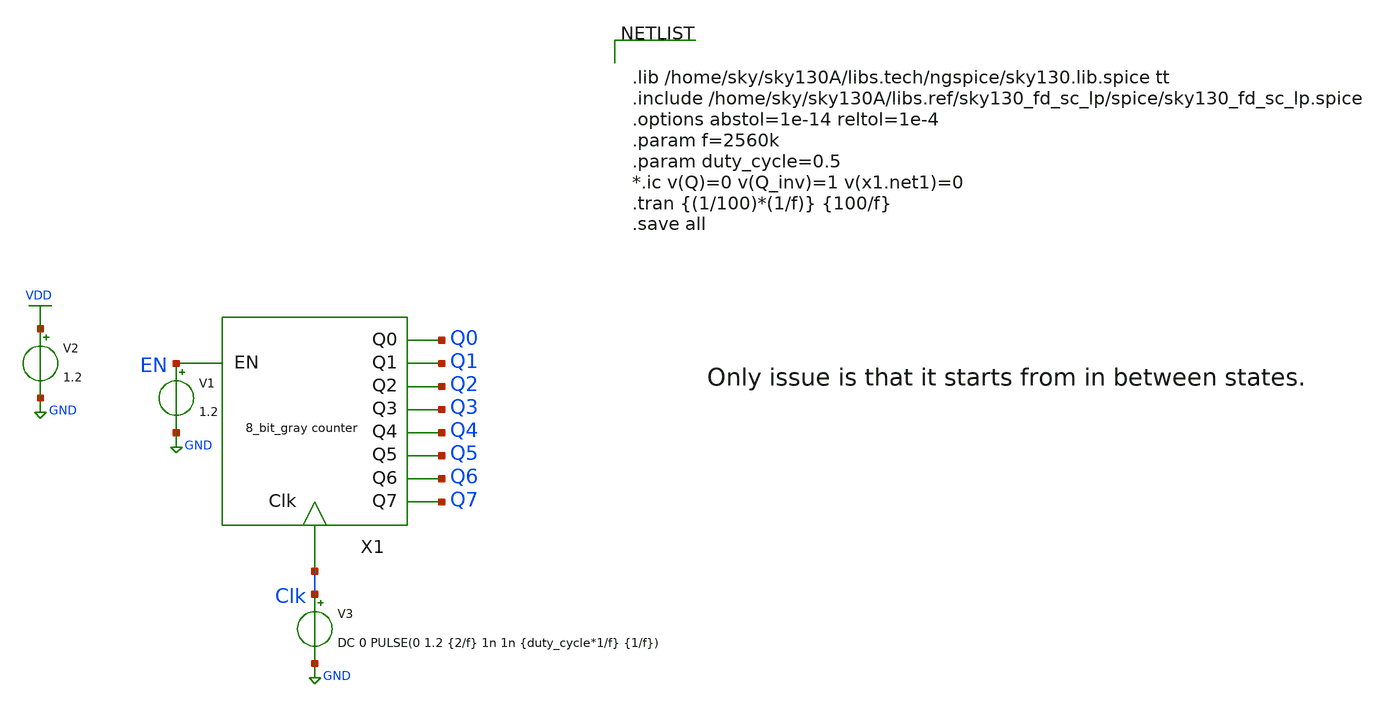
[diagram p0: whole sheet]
** sch_path: xschem/8_bit_gray_counter/8_bit_gray_counter_tb.sch
**.subckt 8_bit_gray_counter_tb
X1 EN Q1 Q6 Clk Q0 Q2 Q3 Q4 Q5 Q7 8_bit_gray_counter
V3 Clk GND DC 0 PULSE(0 1.2 {2/f} 1n 1n {duty_cycle*1/f} {1/f})
V1 EN GND 1.2
V2 VDD GND 1.2
**** begin user architecture code


.lib /home/sky/sky130A/libs.tech/ngspice/sky130.lib.spice tt
.include /home/sky/sky130A/libs.ref/sky130_fd_sc_lp/spice/sky130_fd_sc_lp.spice
.options abstol=1e-14 reltol=1e-4
.param f=2560k
.param duty_cycle=0.5
*.ic v(Q)=0 v(Q_inv)=1 v(x1.net1)=0
.tran {(1/100)*(1/f)} {100/f}
.save all


**** end user architecture code
**.ends

* expanding   symbol:  8_bit_gray_counter/8_bit_gray_counter.sym # of pins=10
** sym_path: xschem/8_bit_gray_counter/8_bit_gray_counter.sym
** sch_path: xschem/8_bit_gray_counter/8_bit_gray_counter.sch
.subckt 8_bit_gray_counter EN Q1 Q6 Clk Q0 Q2 Q3 Q4 Q5 Q7
*.ipin Clk
*.ipin EN
*.opin Q0
*.opin Q1
*.opin Q2
*.opin Q3
*.opin Q4
*.opin Q5
*.opin Q6
*.opin Q7
*.ipin Clk
*.ipin EN
*.opin Q0
*.opin Q1
*.opin Q2
*.opin Q3
*.opin Q4
*.opin Q5
*.opin Q6
*.opin Q7
X1 EN qb0 net7 Clk T_flip_flop
X2 qb0 qb1 net8 Clk T_flip_flop
X3 net1 qb2 net9 Clk T_flip_flop
X4 net2 qb3 net10 Clk T_flip_flop
X5 net3 qb4 net11 Clk T_flip_flop
X6 net4 qb5 net12 Clk T_flip_flop
X7 net5 qb6 net13 Clk T_flip_flop
X8 net6 Q7 net14 Clk T_flip_flop
X10 qb0 qb1 net1 and_gate
X11 net1 qb2 net2 and_gate
X12 net2 qb3 net3 and_gate
X13 net3 qb4 net4 and_gate
X14 net4 qb5 net5 and_gate
X15 net5 qb6 net6 and_gate
X16 qb0 qb1 Q0 exor_gate
X17 qb1 qb2 Q1 exor_gate
X18 qb2 qb3 Q2 exor_gate
X19 qb3 qb4 Q3 exor_gate
X20 qb4 qb5 Q4 exor_gate
X21 qb5 qb6 Q5 exor_gate
X22 qb6 Q7 Q6 exor_gate
X9 EN qb0 net7 Clk T_flip_flop
X23 qb0 qb1 net8 Clk T_flip_flop
X24 net1 qb2 net9 Clk T_flip_flop
X25 net2 qb3 net10 Clk T_flip_flop
X26 net3 qb4 net11 Clk T_flip_flop
X27 net4 qb5 net12 Clk T_flip_flop
X28 net5 qb6 net13 Clk T_flip_flop
X29 net6 Q7 net14 Clk T_flip_flop
X30 qb0 qb1 net1 and_gate
X31 net1 qb2 net2 and_gate
X32 net2 qb3 net3 and_gate
X33 net3 qb4 net4 and_gate
X34 net4 qb5 net5 and_gate
X35 net5 qb6 net6 and_gate
X36 qb0 qb1 Q0 exor_gate
X37 qb1 qb2 Q1 exor_gate
X38 qb2 qb3 Q2 exor_gate
X39 qb3 qb4 Q3 exor_gate
X40 qb4 qb5 Q4 exor_gate
X41 qb5 qb6 Q5 exor_gate
X42 qb6 Q7 Q6 exor_gate
.ends


* expanding   symbol:  T_flip_flop/T_flip_flop.sym # of pins=4
** sym_path: xschem/T_flip_flop/T_flip_flop.sym
** sch_path: xschem/T_flip_flop/T_flip_flop.sch
.subckt T_flip_flop T Q Q_inv Clk
*.ipin T
*.ipin Clk
*.opin Q
*.opin Q_inv
X1 net1 Q Q_inv Clk d_flip_flop
X2 Q T net1 exor_gate
.ends


* expanding   symbol:  and_gate/and_gate.sym # of pins=3
** sym_path: xschem/and_gate/and_gate.sym
** sch_path: xschem/and_gate/and_gate.sch
.subckt and_gate A B out
*.ipin A
*.ipin B
*.opin out
XM1 net1 A net2 GND sky130_fd_pr__nfet_01v8 L=0.18 W=1 nf=1 ad='int((nf+1)/2) * W/nf * 0.29' as='int((nf+2)/2) * W/nf * 0.29'
+ pd='2*int((nf+1)/2) * (W/nf + 0.29)' ps='2*int((nf+2)/2) * (W/nf + 0.29)' nrd='0.29 / W' nrs='0.29 / W'
+ sa=0 sb=0 sd=0 mult=1 m=1
XM2 net1 A VDD VDD sky130_fd_pr__pfet_01v8 L=0.18 W=1 nf=1 ad='int((nf+1)/2) * W/nf * 0.29' as='int((nf+2)/2) * W/nf * 0.29'
+ pd='2*int((nf+1)/2) * (W/nf + 0.29)' ps='2*int((nf+2)/2) * (W/nf + 0.29)' nrd='0.29 / W' nrs='0.29 / W'
+ sa=0 sb=0 sd=0 mult=1 m=1
XM3 net1 B VDD VDD sky130_fd_pr__pfet_01v8 L=0.18 W=1 nf=1 ad='int((nf+1)/2) * W/nf * 0.29' as='int((nf+2)/2) * W/nf * 0.29'
+ pd='2*int((nf+1)/2) * (W/nf + 0.29)' ps='2*int((nf+2)/2) * (W/nf + 0.29)' nrd='0.29 / W' nrs='0.29 / W'
+ sa=0 sb=0 sd=0 mult=1 m=1
XM4 net2 B GND GND sky130_fd_pr__nfet_01v8 L=0.18 W=1 nf=1 ad='int((nf+1)/2) * W/nf * 0.29' as='int((nf+2)/2) * W/nf * 0.29'
+ pd='2*int((nf+1)/2) * (W/nf + 0.29)' ps='2*int((nf+2)/2) * (W/nf + 0.29)' nrd='0.29 / W' nrs='0.29 / W'
+ sa=0 sb=0 sd=0 mult=1 m=1
X1 net1 out inv Wpmos=3 Lpmos=0.18 Wnmos=1 Lnmos=0.18
.ends


* expanding   symbol:  exor_gate/exor_gate.sym # of pins=3
** sym_path: xschem/exor_gate/exor_gate.sym
** sch_path: xschem/exor_gate/exor_gate.sch
.subckt exor_gate A B out
*.ipin A
*.ipin B
*.opin out
XM4 out A net1 GND sky130_fd_pr__nfet_01v8 L=0.18 W=0.5 nf=1 ad='int((nf+1)/2) * W/nf * 0.29' as='int((nf+2)/2) * W/nf * 0.29'
+ pd='2*int((nf+1)/2) * (W/nf + 0.29)' ps='2*int((nf+2)/2) * (W/nf + 0.29)' nrd='0.29 / W' nrs='0.29 / W'
+ sa=0 sb=0 sd=0 mult=1 m=1
XM5 net3 B VDD VDD sky130_fd_pr__pfet_01v8 L=0.18 W=1 nf=1 ad='int((nf+1)/2) * W/nf * 0.29' as='int((nf+2)/2) * W/nf * 0.29'
+ pd='2*int((nf+1)/2) * (W/nf + 0.29)' ps='2*int((nf+2)/2) * (W/nf + 0.29)' nrd='0.29 / W' nrs='0.29 / W'
+ sa=0 sb=0 sd=0 mult=1 m=1
XM1 net1 B GND GND sky130_fd_pr__nfet_01v8 L=0.18 W=0.5 nf=1 ad='int((nf+1)/2) * W/nf * 0.29' as='int((nf+2)/2) * W/nf * 0.29'
+ pd='2*int((nf+1)/2) * (W/nf + 0.29)' ps='2*int((nf+2)/2) * (W/nf + 0.29)' nrd='0.29 / W' nrs='0.29 / W'
+ sa=0 sb=0 sd=0 mult=1 m=1
XM2 out net5 net3 VDD sky130_fd_pr__pfet_01v8 L=0.18 W=1 nf=1 ad='int((nf+1)/2) * W/nf * 0.29' as='int((nf+2)/2) * W/nf * 0.29'
+ pd='2*int((nf+1)/2) * (W/nf + 0.29)' ps='2*int((nf+2)/2) * (W/nf + 0.29)' nrd='0.29 / W' nrs='0.29 / W'
+ sa=0 sb=0 sd=0 mult=1 m=1
XM3 net4 net6 VDD VDD sky130_fd_pr__pfet_01v8 L=0.18 W=1 nf=1 ad='int((nf+1)/2) * W/nf * 0.29' as='int((nf+2)/2) * W/nf * 0.29'
+ pd='2*int((nf+1)/2) * (W/nf + 0.29)' ps='2*int((nf+2)/2) * (W/nf + 0.29)' nrd='0.29 / W' nrs='0.29 / W'
+ sa=0 sb=0 sd=0 mult=1 m=1
XM6 out A net4 VDD sky130_fd_pr__pfet_01v8 L=0.18 W=1 nf=1 ad='int((nf+1)/2) * W/nf * 0.29' as='int((nf+2)/2) * W/nf * 0.29'
+ pd='2*int((nf+1)/2) * (W/nf + 0.29)' ps='2*int((nf+2)/2) * (W/nf + 0.29)' nrd='0.29 / W' nrs='0.29 / W'
+ sa=0 sb=0 sd=0 mult=1 m=1
XM7 out net5 net2 GND sky130_fd_pr__nfet_01v8 L=0.18 W=0.5 nf=1 ad='int((nf+1)/2) * W/nf * 0.29' as='int((nf+2)/2) * W/nf * 0.29'
+ pd='2*int((nf+1)/2) * (W/nf + 0.29)' ps='2*int((nf+2)/2) * (W/nf + 0.29)' nrd='0.29 / W' nrs='0.29 / W'
+ sa=0 sb=0 sd=0 mult=1 m=1
XM8 net2 net6 GND GND sky130_fd_pr__nfet_01v8 L=0.18 W=0.5 nf=1 ad='int((nf+1)/2) * W/nf * 0.29' as='int((nf+2)/2) * W/nf * 0.29'
+ pd='2*int((nf+1)/2) * (W/nf + 0.29)' ps='2*int((nf+2)/2) * (W/nf + 0.29)' nrd='0.29 / W' nrs='0.29 / W'
+ sa=0 sb=0 sd=0 mult=1 m=1
X3 B net6 inv Wpmos=3 Lpmos=0.18 Wnmos=1 Lnmos=0.18
X2 A net5 inv Wpmos=3 Lpmos=0.18 Wnmos=1 Lnmos=0.18
.ends


* expanding   symbol:  D_flip_flop/d_flip_flop.sym # of pins=4
** sym_path: xschem/D_flip_flop/d_flip_flop.sym
** sch_path: xschem/D_flip_flop/d_flip_flop.sch
.subckt d_flip_flop D Q Q_inv Clk
*.ipin D
*.ipin Clk
*.opin Q_inv
*.opin Q
X1 net1 net2 inv Wpmos=3 Lpmos=0.18 Wnmos=1 Lnmos=0.18
X2 net3 Q inv Wpmos=3 Lpmos=0.18 Wnmos=1 Lnmos=0.18
X3 net2 net4 inv Wpmos=3 Lpmos=0.18 Wnmos=1 Lnmos=0.18
X4 Q Q_inv inv Wpmos=3 Lpmos=0.18 Wnmos=1 Lnmos=0.18
X5 D net1 Clk Clk_inv transmission_gate Wpmos=1 Lpmos=0.18 Wnmos=1 Lnmos=0.18
X6 net1 net4 Clk_inv Clk transmission_gate Wpmos=1 Lpmos=0.18 Wnmos=1 Lnmos=0.18
X7 net3 Q_inv Clk Clk_inv transmission_gate Wpmos=1 Lpmos=0.18 Wnmos=1 Lnmos=0.18
X8 net2 net3 Clk_inv Clk transmission_gate Wpmos=1 Lpmos=0.18 Wnmos=1 Lnmos=0.18
X9 Clk Clk_inv inv Wpmos=3 Lpmos=0.18 Wnmos=1 Lnmos=0.18
.ends


* expanding   symbol:  inv/inv.sym # of pins=2
** sym_path: xschem/inv/inv.sym
** sch_path: xschem/inv/inv.sch
.subckt inv in out  Wpmos=3 Lpmos=0.18 Wnmos=1 Lnmos=0.18
*.ipin in
*.iopin out
XM1 out in GND GND sky130_fd_pr__nfet_01v8 L=Lnmos W=Wnmos nf=1 ad='int((nf+1)/2) * W/nf * 0.29' as='int((nf+2)/2) * W/nf * 0.29'
+ pd='2*int((nf+1)/2) * (W/nf + 0.29)' ps='2*int((nf+2)/2) * (W/nf + 0.29)' nrd='0.29 / W' nrs='0.29 / W'
+ sa=0 sb=0 sd=0 mult=1 m=1
XM2 out in VDD VDD sky130_fd_pr__pfet_01v8 L=Lpmos W=Wpmos nf=1 ad='int((nf+1)/2) * W/nf * 0.29' as='int((nf+2)/2) * W/nf * 0.29'
+ pd='2*int((nf+1)/2) * (W/nf + 0.29)' ps='2*int((nf+2)/2) * (W/nf + 0.29)' nrd='0.29 / W' nrs='0.29 / W'
+ sa=0 sb=0 sd=0 mult=1 m=1
.ends


* expanding   symbol:  transmission_gate/transmission_gate.sym # of pins=4
** sym_path: xschem/transmission_gate/transmission_gate.sym
** sch_path: xschem/transmission_gate/transmission_gate.sch
.subckt transmission_gate in out ctrl_ ctrl  Wpmos=1 Lpmos=0.18 Wnmos=1 Lnmos=0.18
*.iopin in
*.iopin out
*.ipin ctrl_
*.ipin ctrl
XM1 in ctrl out GND sky130_fd_pr__nfet_01v8 L=Lnmos W=Wnmos nf=1 ad='int((nf+1)/2) * W/nf * 0.29' as='int((nf+2)/2) * W/nf * 0.29'
+ pd='2*int((nf+1)/2) * (W/nf + 0.29)' ps='2*int((nf+2)/2) * (W/nf + 0.29)' nrd='0.29 / W' nrs='0.29 / W'
+ sa=0 sb=0 sd=0 mult=1 m=1
XM2 out ctrl_ in VDD sky130_fd_pr__pfet_01v8 L=Lpmos W=Wpmos nf=1 ad='int((nf+1)/2) * W/nf * 0.29' as='int((nf+2)/2) * W/nf * 0.29'
+ pd='2*int((nf+1)/2) * (W/nf + 0.29)' ps='2*int((nf+2)/2) * (W/nf + 0.29)' nrd='0.29 / W' nrs='0.29 / W'
+ sa=0 sb=0 sd=0 mult=1 m=1
.ends

.GLOBAL GND
.GLOBAL VDD
.end
